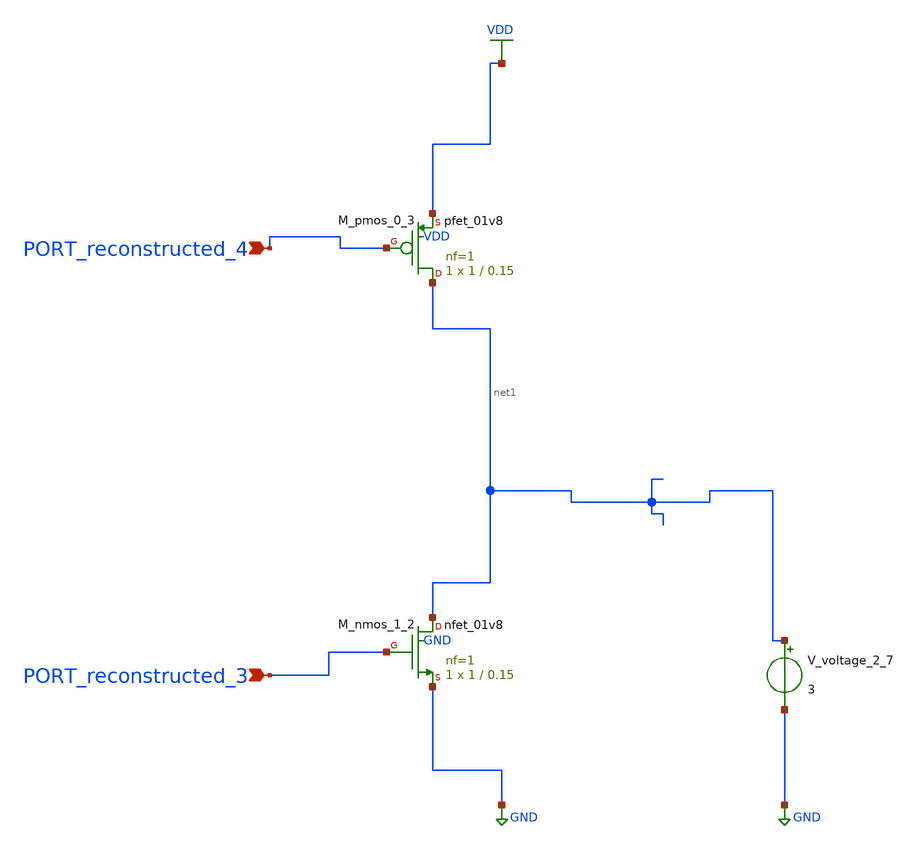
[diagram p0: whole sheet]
** sch_path: schematics/AMSNet/166.sch
**.subckt 166 PORT_reconstructed_3 PORT_reconstructed_4
*.ipin PORT_reconstructed_3
*.ipin PORT_reconstructed_4
XM_nmos_1_2 net1 PORT_reconstructed_3 GND GND sky130_fd_pr__nfet_01v8 L=0.15 W=1 nf=1 ad='int((1 + 1)/2) * 1 / 1 * 0.29'
+ as='int((1 + 2)/2) * 1 / 1 * 0.29' pd='2*int((1 + 1)/2) * (1 / 1 + 0.29)' ps='2*int((1 + 2)/2) * (1 / 1 + 0.29)'
+ nrd='0.29 / 1 ' nrs='0.29 / 1 ' sa=0 sb=0 sd=0 mult=1 m=1
XM_pmos_0_3 net1 PORT_reconstructed_4 VDD VDD sky130_fd_pr__pfet_01v8 L=0.15 W=1 nf=1 ad='int((1 + 1)/2) * 1 / 1 * 0.29'
+ as='int((1 + 2)/2) * 1 / 1 * 0.29' pd='2*int((1 + 1)/2) * (1 / 1 + 0.29)' ps='2*int((1 + 2)/2) * (1 / 1 + 0.29)'
+ nrd='0.29 / 1 ' nrs='0.29 / 1 ' sa=0 sb=0 sd=0 mult=1 m=1
V_voltage_2_7 net1 GND 3
**.ends
.GLOBAL GND
.GLOBAL VDD
.end
